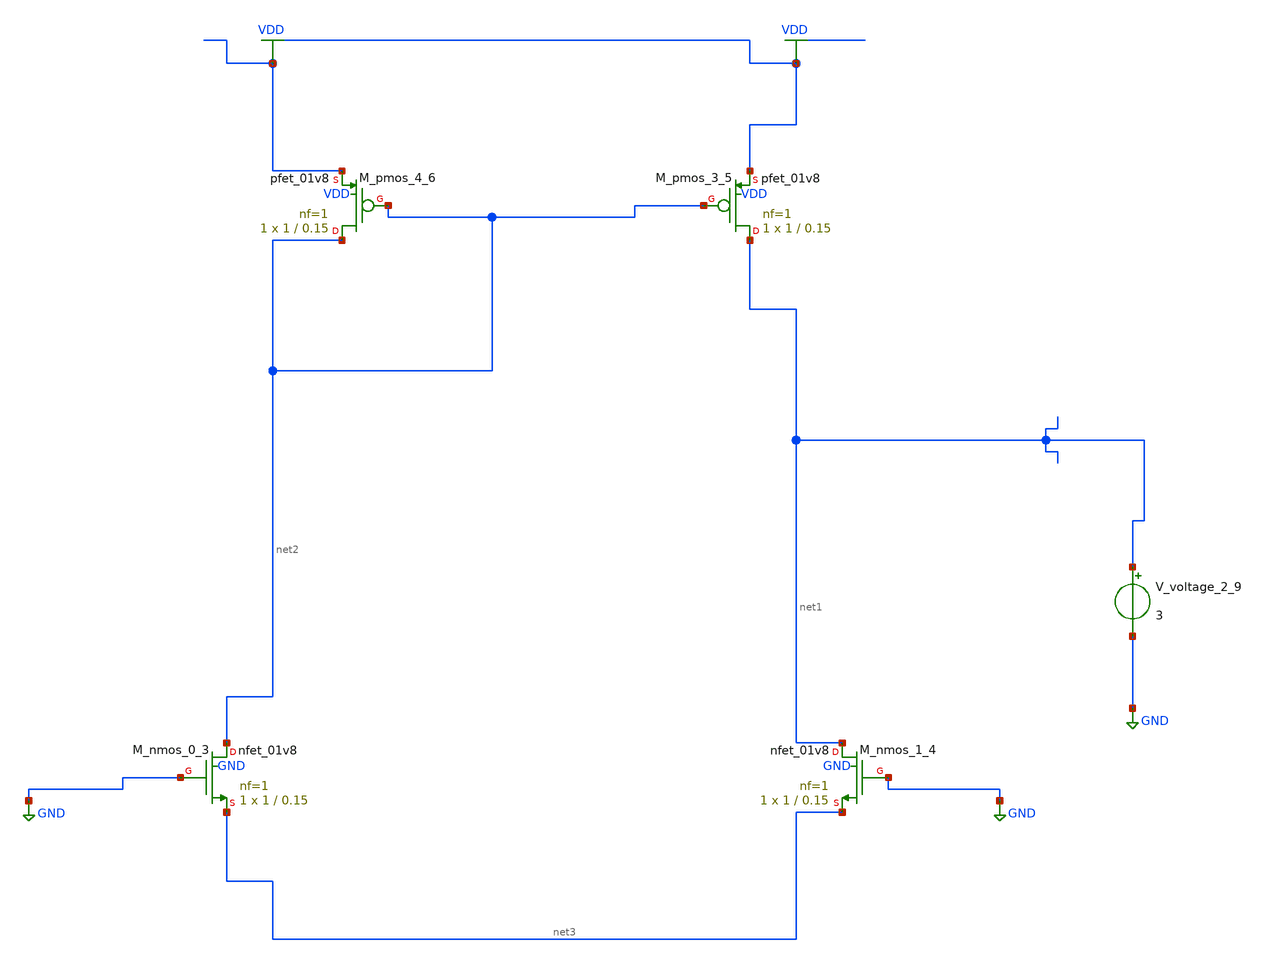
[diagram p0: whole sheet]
** sch_path: schematics/AMSNet/283.sch
**.subckt 283
XM_nmos_0_3 net2 GND net3 GND sky130_fd_pr__nfet_01v8 L=0.15 W=1 nf=1 ad='int((1 + 1)/2) * 1 / 1 * 0.29'
+ as='int((1 + 2)/2) * 1 / 1 * 0.29' pd='2*int((1 + 1)/2) * (1 / 1 + 0.29)' ps='2*int((1 + 2)/2) * (1 / 1 + 0.29)'
+ nrd='0.29 / 1 ' nrs='0.29 / 1 ' sa=0 sb=0 sd=0 mult=1 m=1
XM_nmos_1_4 net1 GND net3 GND sky130_fd_pr__nfet_01v8 L=0.15 W=1 nf=1 ad='int((1 + 1)/2) * 1 / 1 * 0.29'
+ as='int((1 + 2)/2) * 1 / 1 * 0.29' pd='2*int((1 + 1)/2) * (1 / 1 + 0.29)' ps='2*int((1 + 2)/2) * (1 / 1 + 0.29)'
+ nrd='0.29 / 1 ' nrs='0.29 / 1 ' sa=0 sb=0 sd=0 mult=1 m=1
XM_pmos_3_5 net1 net2 VDD VDD sky130_fd_pr__pfet_01v8 L=0.15 W=1 nf=1 ad='int((1 + 1)/2) * 1 / 1 * 0.29'
+ as='int((1 + 2)/2) * 1 / 1 * 0.29' pd='2*int((1 + 1)/2) * (1 / 1 + 0.29)' ps='2*int((1 + 2)/2) * (1 / 1 + 0.29)'
+ nrd='0.29 / 1 ' nrs='0.29 / 1 ' sa=0 sb=0 sd=0 mult=1 m=1
XM_pmos_4_6 net2 net2 VDD VDD sky130_fd_pr__pfet_01v8 L=0.15 W=1 nf=1 ad='int((1 + 1)/2) * 1 / 1 * 0.29'
+ as='int((1 + 2)/2) * 1 / 1 * 0.29' pd='2*int((1 + 1)/2) * (1 / 1 + 0.29)' ps='2*int((1 + 2)/2) * (1 / 1 + 0.29)'
+ nrd='0.29 / 1 ' nrs='0.29 / 1 ' sa=0 sb=0 sd=0 mult=1 m=1
V_voltage_2_9 net1 GND 3
**.ends
.GLOBAL GND
.GLOBAL VDD
.end
